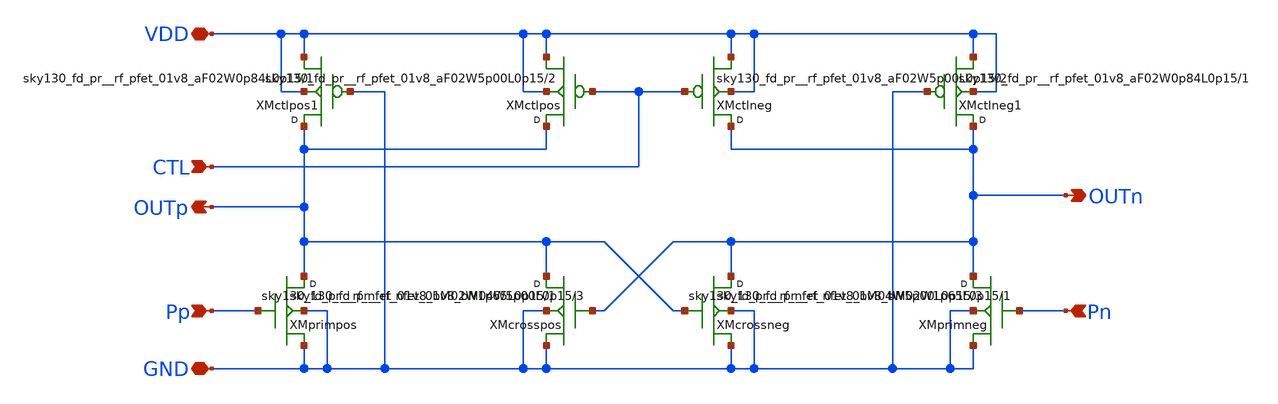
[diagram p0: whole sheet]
** sch_path: design/vco_delaycell/vco_delaycell.sch
**.subckt vco_delaycell Pp Pn OUTn OUTp VDD GND CTL
*.ipin Pp
*.ipin Pn
*.opin OUTn
*.opin OUTp
*.iopin VDD
*.iopin GND
*.ipin CTL
XXMprimpos OUTp Pp GND GND sky130_fd_pr__rf_nfet_01v8_bM04W5p00L0p15 m=3
XXMcrossneg OUTn OUTp GND GND sky130_fd_pr__rf_nfet_01v8_bM02W1p65L0p15 m=1
XXMctlneg OUTn CTL VDD VDD sky130_fd_pr__rf_pfet_01v8_aF02W5p00L0p15 m=2
XXMctlpos OUTp CTL VDD VDD sky130_fd_pr__rf_pfet_01v8_aF02W5p00L0p15 m=2
XXMcrosspos OUTp OUTn GND GND sky130_fd_pr__rf_nfet_01v8_bM02W1p65L0p15 m=1
XXMprimneg OUTn Pn GND GND sky130_fd_pr__rf_nfet_01v8_bM04W5p00L0p15 m=3
XXMctlpos1 OUTp GND VDD VDD sky130_fd_pr__rf_pfet_01v8_aF02W0p84L0p15 m=1
XXMctlneg1 OUTn GND VDD VDD sky130_fd_pr__rf_pfet_01v8_aF02W0p84L0p15 m=1
**.ends
.end
